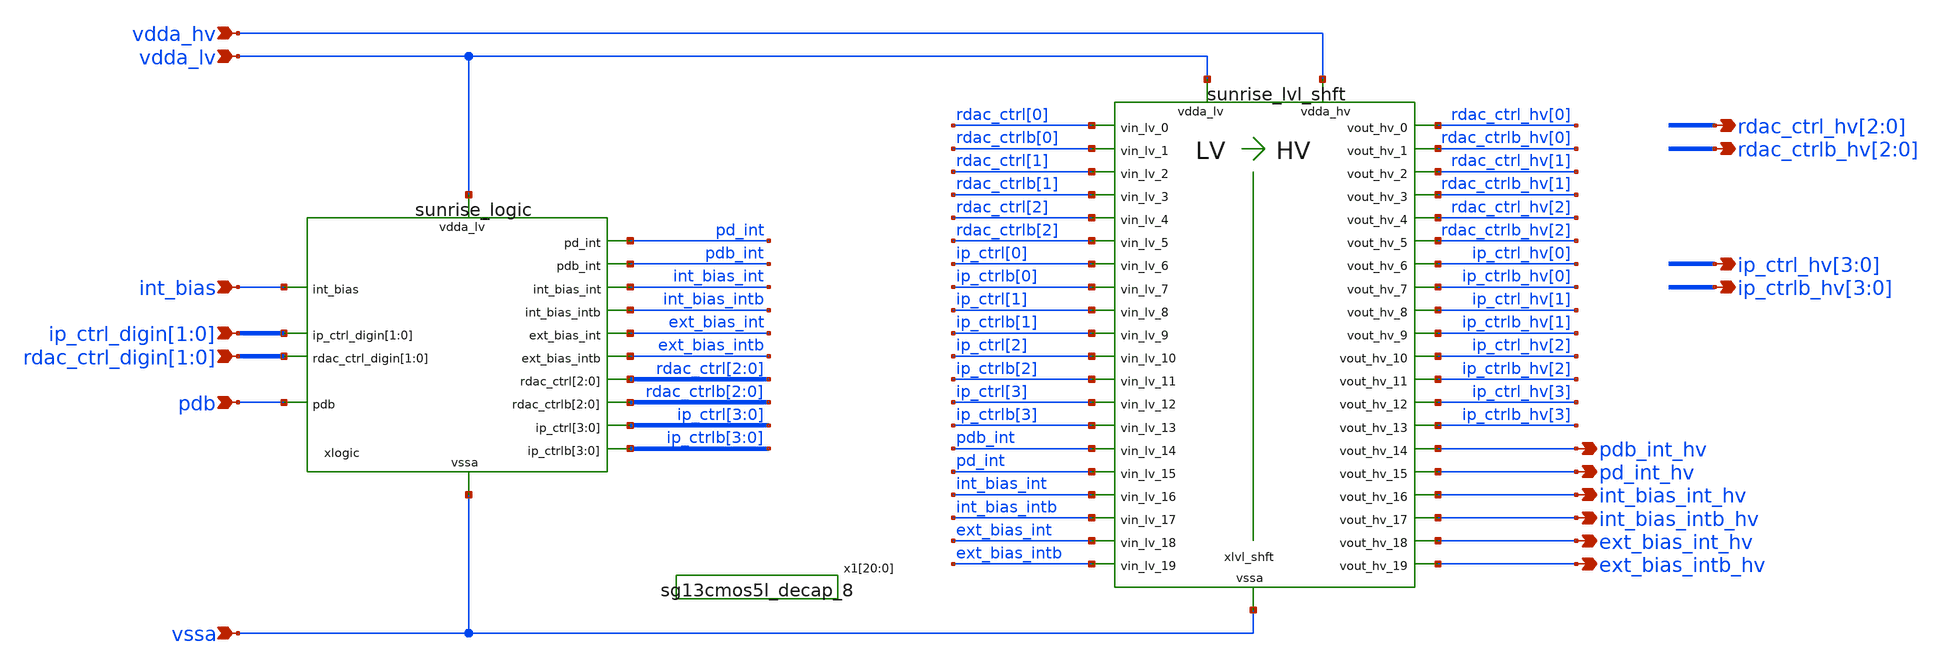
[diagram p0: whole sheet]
** sch_path: Schematics_Layout/sunrise_logic_wlvl_shft/sunrise_logic_wlvl_shft.sch
**.subckt sunrise_logic_wlvl_shft int_bias pdb ip_ctrl_digin[1],ip_ctrl_digin[0]
*+ rdac_ctrl_digin[1],rdac_ctrl_digin[0] vdda_lv vdda_hv vssa rdac_ctrl_hv[2],rdac_ctrl_hv[1],rdac_ctrl_hv[0]
*+ rdac_ctrlb_hv[2],rdac_ctrlb_hv[1],rdac_ctrlb_hv[0] ip_ctrl_hv[3],ip_ctrl_hv[2],ip_ctrl_hv[1],ip_ctrl_hv[0]
*+ ip_ctrlb_hv[3],ip_ctrlb_hv[2],ip_ctrlb_hv[1],ip_ctrlb_hv[0] pdb_int_hv pd_int_hv int_bias_int_hv int_bias_intb_hv ext_bias_int_hv ext_bias_intb_hv
*.ipin int_bias
*.ipin pdb
*.ipin ip_ctrl_digin[1],ip_ctrl_digin[0]
*.ipin rdac_ctrl_digin[1],rdac_ctrl_digin[0]
*.ipin vdda_lv
*.ipin vdda_hv
*.ipin vssa
*.opin rdac_ctrl_hv[2],rdac_ctrl_hv[1],rdac_ctrl_hv[0]
*.opin rdac_ctrlb_hv[2],rdac_ctrlb_hv[1],rdac_ctrlb_hv[0]
*.opin ip_ctrl_hv[3],ip_ctrl_hv[2],ip_ctrl_hv[1],ip_ctrl_hv[0]
*.opin ip_ctrlb_hv[3],ip_ctrlb_hv[2],ip_ctrlb_hv[1],ip_ctrlb_hv[0]
*.opin pdb_int_hv
*.opin pd_int_hv
*.opin int_bias_int_hv
*.opin int_bias_intb_hv
*.opin ext_bias_int_hv
*.opin ext_bias_intb_hv
xlogic vdda_lv pd_int pdb_int int_bias_int int_bias_intb int_bias pdb ext_bias_int ext_bias_intb
+ rdac_ctrl_digin[1] rdac_ctrl_digin[0] rdac_ctrl[2] rdac_ctrl[1] rdac_ctrl[0] ip_ctrl[3] ip_ctrl[2] ip_ctrl[1]
+ ip_ctrl[0] ip_ctrl_digin[1] ip_ctrl_digin[0] rdac_ctrlb[2] rdac_ctrlb[1] rdac_ctrlb[0] ip_ctrlb[3] ip_ctrlb[2]
+ ip_ctrlb[1] ip_ctrlb[0] vssa sunrise_logic
xlvl_shft vdda_hv vdda_lv rdac_ctrl[0] rdac_ctrl_hv[0] vssa rdac_ctrlb_hv[0] rdac_ctrlb[0]
+ rdac_ctrl_hv[1] rdac_ctrl[1] rdac_ctrlb[1] rdac_ctrlb_hv[1] rdac_ctrl_hv[2] rdac_ctrl[2] rdac_ctrlb[2]
+ rdac_ctrlb_hv[2] ip_ctrl_hv[0] ip_ctrl[0] ip_ctrlb_hv[0] ip_ctrlb[0] ip_ctrl[1] ip_ctrl_hv[1] ip_ctrlb_hv[1]
+ ip_ctrlb[1] ip_ctrl_hv[2] ip_ctrl[2] ip_ctrlb_hv[2] ip_ctrlb[2] ip_ctrl[3] ip_ctrl_hv[3] ip_ctrlb_hv[3]
+ ip_ctrlb[3] pdb_int_hv pdb_int pd_int_hv pd_int int_bias_int int_bias_int_hv int_bias_intb_hv int_bias_intb
+ ext_bias_int ext_bias_int_hv ext_bias_intb_hv ext_bias_intb sunrise_lvl_shft
x1[20] vdda_lv vssa sg13cmos5l_decap_8
x1[19] vdda_lv vssa sg13cmos5l_decap_8
x1[18] vdda_lv vssa sg13cmos5l_decap_8
x1[17] vdda_lv vssa sg13cmos5l_decap_8
x1[16] vdda_lv vssa sg13cmos5l_decap_8
x1[15] vdda_lv vssa sg13cmos5l_decap_8
x1[14] vdda_lv vssa sg13cmos5l_decap_8
x1[13] vdda_lv vssa sg13cmos5l_decap_8
x1[12] vdda_lv vssa sg13cmos5l_decap_8
x1[11] vdda_lv vssa sg13cmos5l_decap_8
x1[10] vdda_lv vssa sg13cmos5l_decap_8
x1[9] vdda_lv vssa sg13cmos5l_decap_8
x1[8] vdda_lv vssa sg13cmos5l_decap_8
x1[7] vdda_lv vssa sg13cmos5l_decap_8
x1[6] vdda_lv vssa sg13cmos5l_decap_8
x1[5] vdda_lv vssa sg13cmos5l_decap_8
x1[4] vdda_lv vssa sg13cmos5l_decap_8
x1[3] vdda_lv vssa sg13cmos5l_decap_8
x1[2] vdda_lv vssa sg13cmos5l_decap_8
x1[1] vdda_lv vssa sg13cmos5l_decap_8
x1[0] vdda_lv vssa sg13cmos5l_decap_8
**.ends
.end
